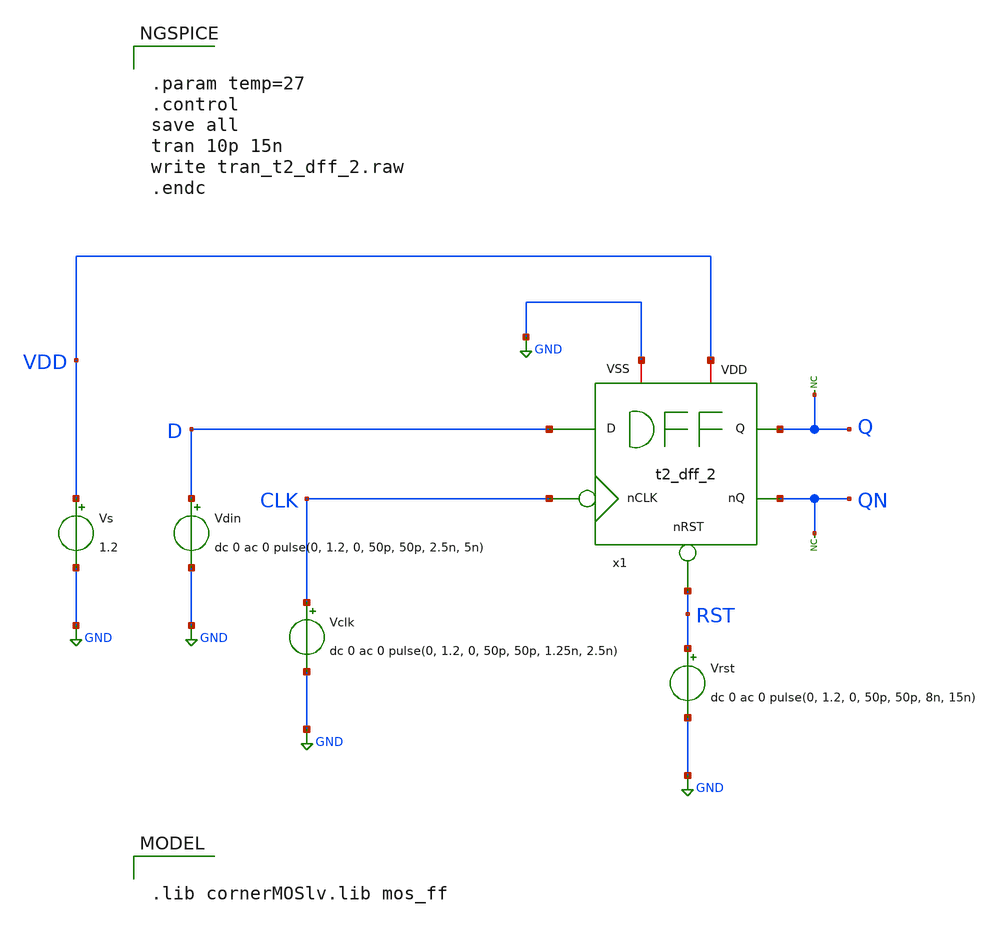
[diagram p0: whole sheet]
** sch_path: Team 2 Design/design_data/xschem/t2_dff_2_tb.sch
**.subckt t2_dff_2_tb
Vs VDD GND 1.2
* noconn Q
* noconn QN
Vdin D GND dc 0 ac 0 pulse(0, 1.2, 0, 50p, 50p, 2.5n, 5n)
Vclk CLK GND dc 0 ac 0 pulse(0, 1.2, 0, 50p, 50p, 1.25n, 2.5n)
Vrst RST GND dc 0 ac 0 pulse(0, 1.2, 0, 50p, 50p, 8n, 15n)
x1 D CLK Q VDD QN RST GND t2_dff_2
**** begin user architecture code


.param temp=27
.control
save all
tran 10p 15n
write tran_t2_dff_2.raw
.endc



.lib cornerMOSlv.lib mos_ff

**** end user architecture code
**.ends

* expanding   symbol:  t2_dff_2.sym # of pins=7
** sym_path: Team 2 Design/design_data/xschem/t2_dff_2.sym
** sch_path: Team 2 Design/design_data/xschem/t2_dff_2.sch
.subckt t2_dff_2 D nCLK Q VDD nQ nRST VSS
*.iopin VSS
*.ipin D
*.ipin nRST
*.opin Q
*.iopin VDD
*.opin nQ
*.ipin nCLK
XM1 net1 D VDD VDD sg13_lv_pmos w=0.3u l=0.15u ng=1 m=1 mm_ok=1
XM2 net2 CLK net1 VDD sg13_lv_pmos w=0.3u l=0.15u ng=1 m=1 mm_ok=1
XM3 net2 D VSS VSS sg13_lv_nmos w=0.15u l=0.13u ng=1 m=1 mm_ok=1
XM4 net3 CLK VDD VDD sg13_lv_pmos w=0.3u l=0.15u ng=1 m=1 mm_ok=1
XM6 net4 CLK VSS VSS sg13_lv_nmos w=0.15u l=0.13u ng=1 m=1 mm_ok=1
XM5 net3 net2 net4 VSS sg13_lv_nmos w=0.15u l=0.13u ng=1 m=1 mm_ok=1
XM7 nQ net3 VDD VDD sg13_lv_pmos w=0.3u l=0.15u ng=1 m=1 mm_ok=1
XM8 net5 net3 VSS VSS sg13_lv_nmos w=0.15u l=0.13u ng=1 m=1 mm_ok=1
XM9 nQ CLK net5 VSS sg13_lv_nmos w=0.15u l=0.13u ng=1 m=1 mm_ok=1
XM10 nQ nRST VDD VDD sg13_lv_pmos w=0.3u l=0.15u ng=1 m=1 mm_ok=1
XM11 Q nQ VDD VDD sg13_lv_pmos w=0.3u l=0.15u ng=1 m=1 mm_ok=1
XM12 Q nQ VSS VSS sg13_lv_nmos w=0.15u l=0.13u ng=1 m=1 mm_ok=1
x1 VDD nCLK CLK VSS t2_inverter
.ends


* expanding   symbol:  t2_inverter.sym # of pins=4
** sym_path: Team 2 Design/design_data/xschem/t2_inverter.sym
** sch_path: Team 2 Design/design_data/xschem/t2_inverter.sch
.subckt t2_inverter VP A Y VN
*.iopin VP
*.iopin VN
*.ipin A
*.opin Y
XM2 Y A VP VP sg13_lv_pmos w=0.3u l=0.13u ng=1 m=1 mm_ok=1
XM1 Y A VN VN sg13_lv_nmos w=0.15u l=0.13u ng=1 m=1 mm_ok=1
.ends

.GLOBAL GND
.end
